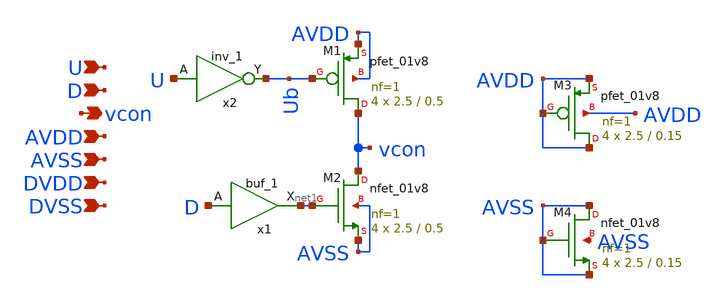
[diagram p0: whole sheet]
** sch_path: xschem/charge_pump.sch
**.subckt charge_pump U D vcon AVDD AVSS DVDD DVSS
*.ipin U
*.ipin D
*.opin vcon
*.ipin AVDD
*.ipin AVSS
*.ipin DVDD
*.ipin DVSS
XM1 vcon Ub AVDD AVDD sky130_fd_pr__pfet_01v8 L=0.5 W=2.5 nf=1 ad='int((nf+1)/2) * W/nf * 0.29' as='int((nf+2)/2) * W/nf * 0.29'
+ pd='2*int((nf+1)/2) * (W/nf + 0.29)' ps='2*int((nf+2)/2) * (W/nf + 0.29)' nrd='0.29 / W' nrs='0.29 / W'
+ sa=0 sb=0 sd=0 mult=4 m=4
XM2 vcon net1 AVSS AVSS sky130_fd_pr__nfet_01v8 L=0.5 W=2.5 nf=1 ad='int((nf+1)/2) * W/nf * 0.29' as='int((nf+2)/2) * W/nf * 0.29'
+ pd='2*int((nf+1)/2) * (W/nf + 0.29)' ps='2*int((nf+2)/2) * (W/nf + 0.29)' nrd='0.29 / W' nrs='0.29 / W'
+ sa=0 sb=0 sd=0 mult=4 m=4
x1 D DVSS DVSS DVDD DVDD net1 sky130_fd_sc_hd__buf_1
x2 U DVSS DVSS DVDD DVDD Ub sky130_fd_sc_hd__inv_1
XM3 AVDD AVDD AVDD AVDD sky130_fd_pr__pfet_01v8 L=0.15 W=2.5 nf=1 ad='int((nf+1)/2) * W/nf * 0.29' as='int((nf+2)/2) * W/nf * 0.29'
+ pd='2*int((nf+1)/2) * (W/nf + 0.29)' ps='2*int((nf+2)/2) * (W/nf + 0.29)' nrd='0.29 / W' nrs='0.29 / W'
+ sa=0 sb=0 sd=0 mult=4 m=4
XM4 AVSS AVSS AVSS AVSS sky130_fd_pr__nfet_01v8 L=0.15 W=2.5 nf=1 ad='int((nf+1)/2) * W/nf * 0.29' as='int((nf+2)/2) * W/nf * 0.29'
+ pd='2*int((nf+1)/2) * (W/nf + 0.29)' ps='2*int((nf+2)/2) * (W/nf + 0.29)' nrd='0.29 / W' nrs='0.29 / W'
+ sa=0 sb=0 sd=0 mult=4 m=4
**.ends
.end
